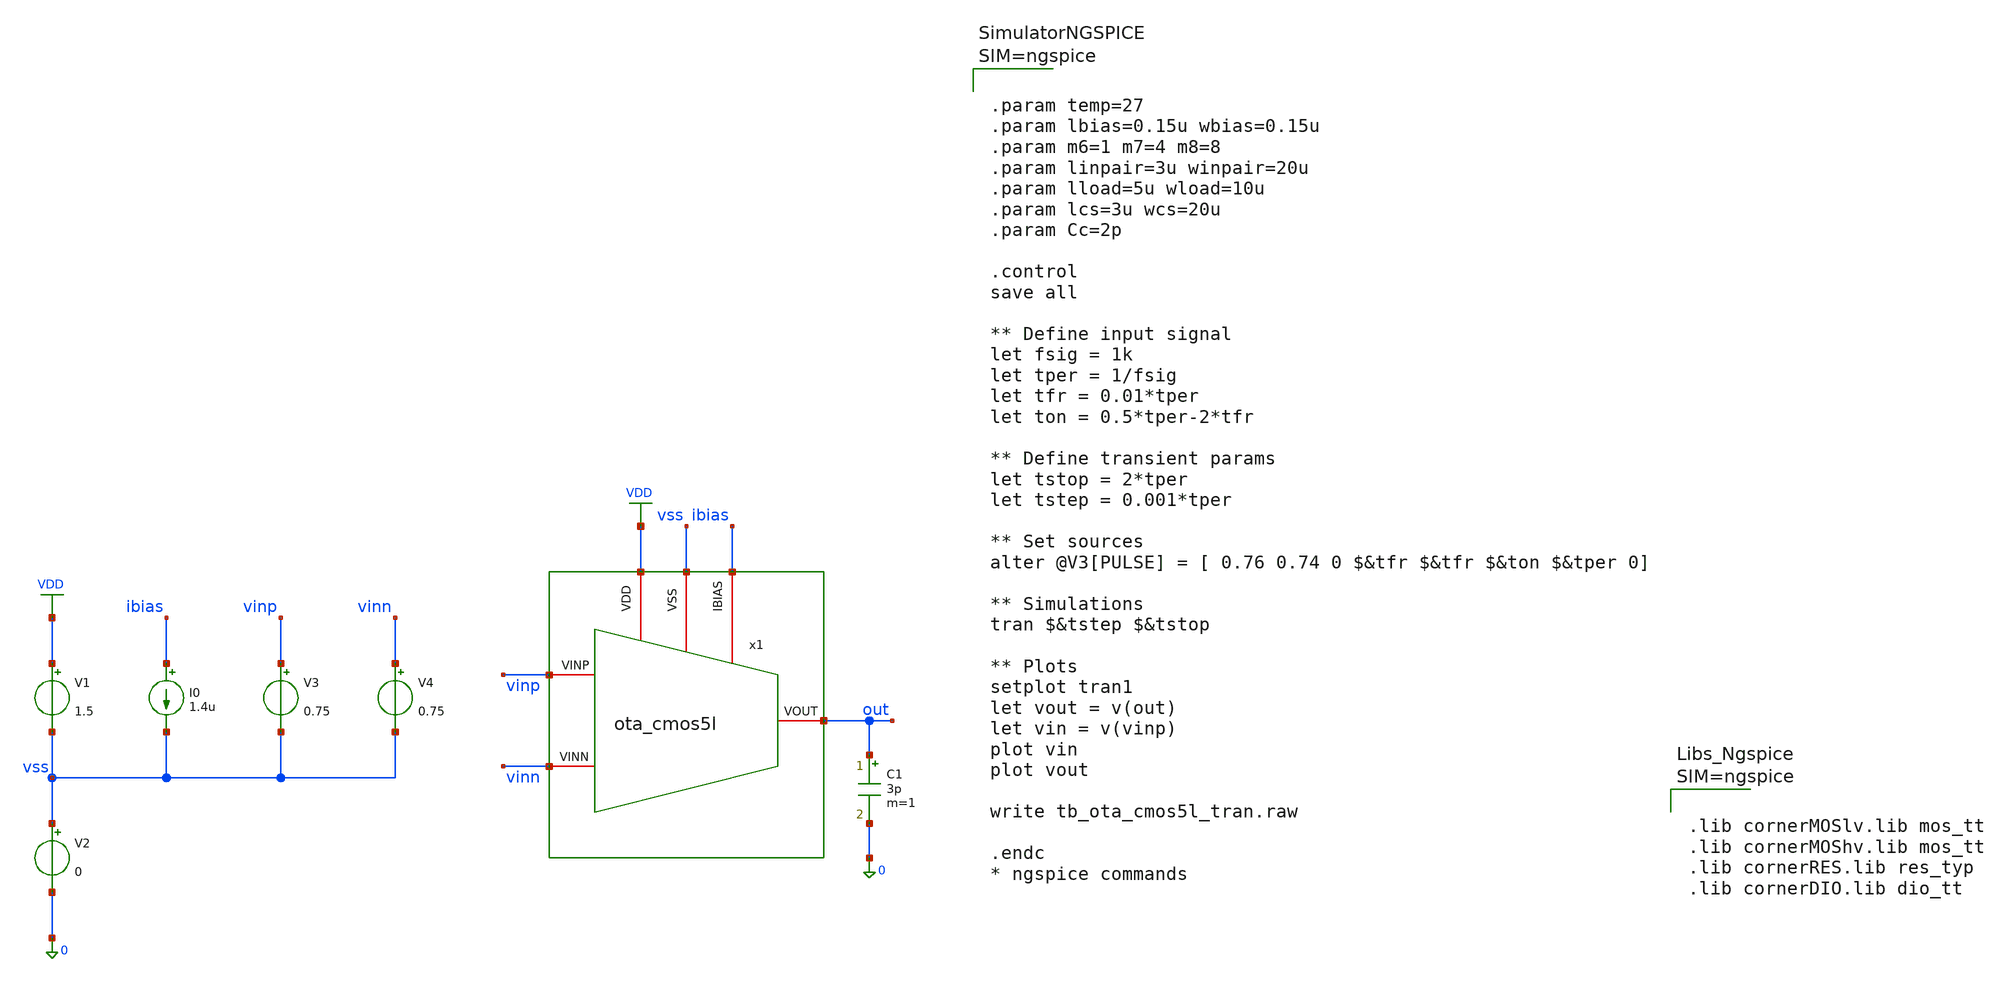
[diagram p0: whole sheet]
** sch_path: xschem/ota_cmos5l/tb/tb_ota_cmos5l_tran/tb_ota_cmos5l_tran.sch
**.subckt tb_ota_cmos5l_tran
x1 vss ibias VDD vinn vinp out ota_cmos5l
C1 out 0 3p m=1
I0 ibias vss 1.4u
V1 VDD vss 1.5
V2 vss 0 0
V3 vinp vss 0.75
V4 vinn vss 0.75
**** begin user architecture code



.param temp=27
.param lbias=0.15u wbias=0.15u
.param m6=1 m7=4 m8=8
.param linpair=3u winpair=20u
.param lload=5u wload=10u
.param lcs=3u wcs=20u
.param Cc=2p

.control
save all

** Define input signal
let fsig = 1k
let tper = 1/fsig
let tfr = 0.01*tper
let ton = 0.5*tper-2*tfr

** Define transient params
let tstop = 2*tper
let tstep = 0.001*tper

** Set sources
alter @V3[PULSE] = [ 0.76 0.74 0 $&tfr $&tfr $&ton $&tper 0]

** Simulations
tran $&tstep $&tstop

** Plots
setplot tran1
let vout = v(out)
let vin = v(vinp)
plot vin
plot vout

write tb_ota_cmos5l_tran.raw

.endc
* ngspice commands






.lib cornerMOSlv.lib mos_tt
.lib cornerMOShv.lib mos_tt
.lib cornerRES.lib res_typ
.lib cornerDIO.lib dio_tt



**** end user architecture code
**.ends

* expanding   symbol:
*+  /foss/designs/Programmable-Instrumentation-Amplifier-IP/designs/libs/core_analog/ota_cmos5l/ota_cmos5l.sym # of pins=6
** sym_path: /foss/designs/Programmable-Instrumentation-Amplifier-IP/designs/libs/core_analog/ota_cmos5l/ota_cmos5l.sym
** sch_path: /foss/designs/Programmable-Instrumentation-Amplifier-IP/designs/libs/core_analog/ota_cmos5l/ota_cmos5l.sch
.subckt ota_cmos5l VSS IBIAS VDD VINN VINP VOUT
*.iopin IBIAS
*.iopin VDD
*.iopin VSS
*.iopin VOUT
*.iopin VINP
*.iopin VINN
XM6 net1 net1 vdd vdd sg13_lv_pmos w={wbias} l={lbias} ng=1 m={m6} mm_ok=1
XM7 net5 net1 vdd vdd sg13_lv_pmos w={wbias} l={lbias} ng=1 m={m7} mm_ok=1
XM8 net6 net1 vdd vdd sg13_lv_pmos w={wbias} l={lbias} ng=1 m={m8} mm_ok=1
XM1 net7 VINN net2 vdd sg13_lv_pmos w={winpair} l={linpair} ng=1 m=1 mm_ok=1
XM2 net8 VINP net2 vdd sg13_lv_pmos w={winpair} l={linpair} ng=1 m=1 mm_ok=1
XM3 net3 net3 gnd gnd sg13_lv_nmos w={wload} l={lload} ng=1 m=1 mm_ok=1
XM4 net4 net3 gnd gnd sg13_lv_nmos w={wload} l={lload} ng=1 m=1 mm_ok=1
XM5 net9 net4 gnd gnd sg13_lv_nmos w={wcs} l={lcs} ng=1 m=1 mm_ok=1
C1 net10 net9 {Cc} m=1
XR1 net4 net10 sub! rhigh w=0.5e-6 l=1.95e-6 m=1 b=0 mm_ok=1
**** begin user architecture code



.include ota_cmos5l.save
.param temp=27
.param lbias=0.15u wbias=0.15u
.param m6=1 m7=4 m8=10
.param linpair=3u winpair=20u
.param lload=0.5u wload=0.42u
.param lcs=5u wcs=19.13u
.param Cc=1.5p
.control
op
write ota_cmos5l.raw
.endc



**** end user architecture code
**** begin user architecture code



.lib cornerMOSlv.lib mos_tt
.lib cornerMOShv.lib mos_tt
.lib cornerRES.lib res_typ
.lib cornerDIO.lib dio_tt



**** end user architecture code
VIBIAS net1 ibias 0
.save i(vibias)
VID7 net5 net2 0
.save i(vid7)
VID8 net6 VOUT 0
.save i(vid8)
VIVDD VDD vdd 0
.save i(vivdd)
.save v(vinp)
.save v(vinn)
.save v(vout)
VID1 net7 net3 0
.save i(vid1)
VID2 net8 net4 0
.save i(vid2)
VID5 VOUT net9 0
.save i(vid5)
.ends

.GLOBAL VDD
.end
